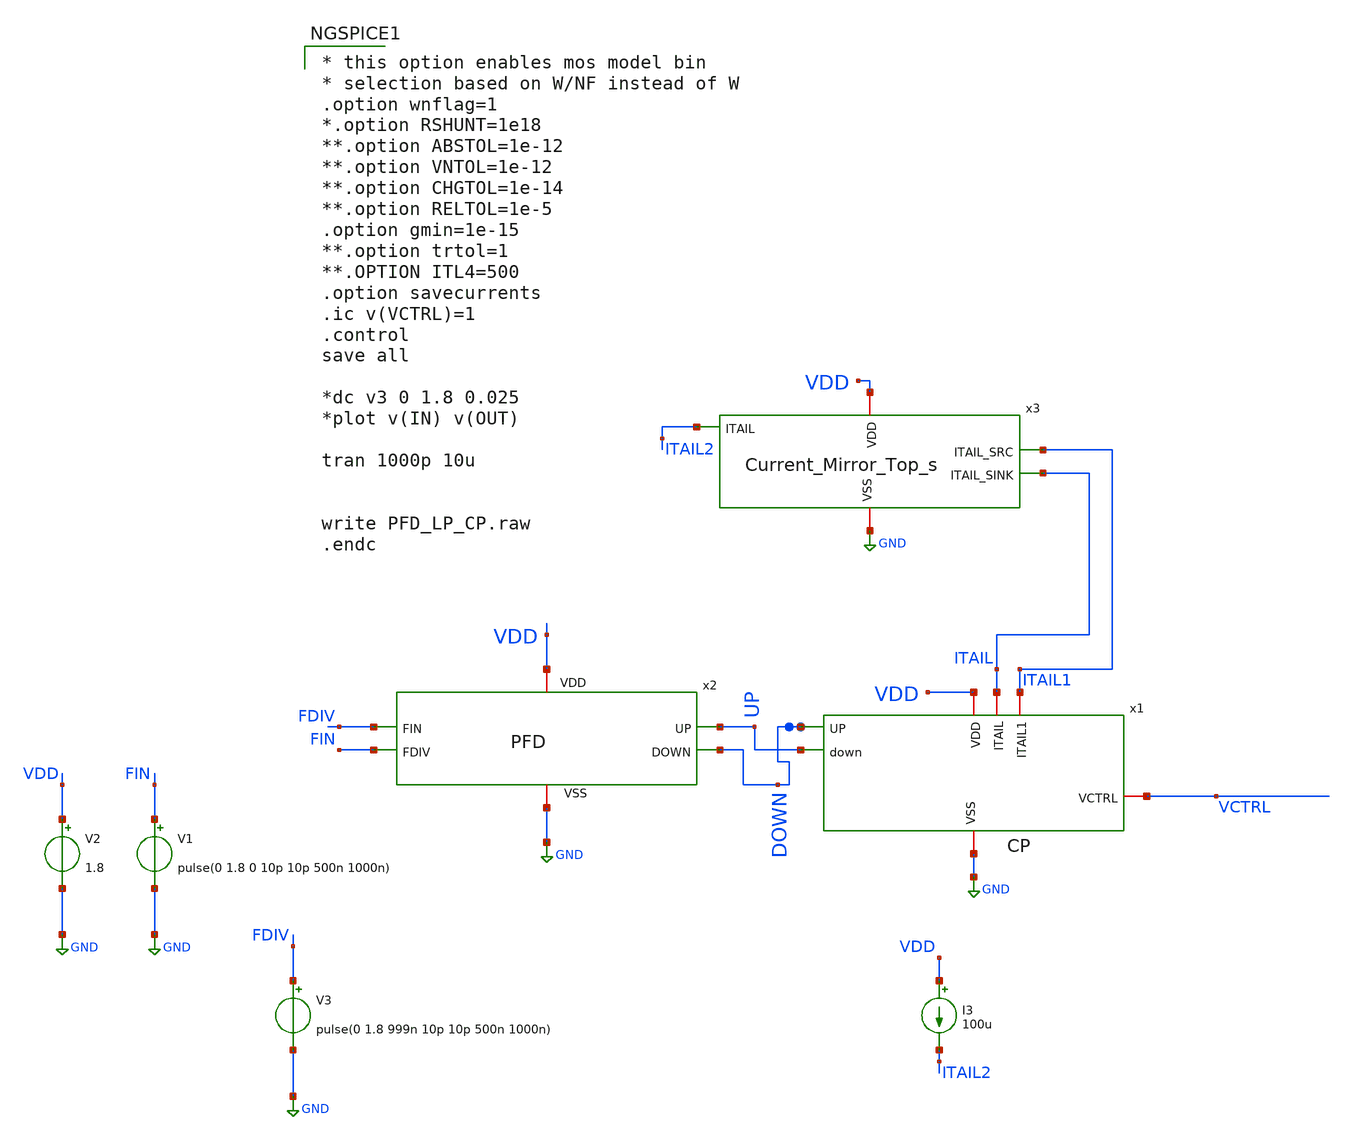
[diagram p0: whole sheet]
** sch_path: Xschem/PLL_TOP/PFD_LP_CP.sch
**.subckt PFD_LP_CP
x1 VDD ITAIL ITAIL1 VCTRL DOWN UP GND CP
V2 VDD GND 1.8
V1 FIN GND pulse(0 1.8 0 10p 10p 500n 1000n)
V3 FDIV GND pulse(0 1.8 999n 10p 10p 500n 1000n)
x2 VDD GND FDIV FIN UP DOWN PFD
x3 VDD ITAIL2 ITAIL1 ITAIL GND Current_Mirror_Top_s
I3 VDD ITAIL2 100u
**** begin user architecture code

** opencircuitdesign pdks install
.lib $::SKYWATER_MODELS/sky130.lib.spice tt



* this option enables mos model bin
* selection based on W/NF instead of W
.option wnflag=1
*.option RSHUNT=1e18
**.option ABSTOL=1e-12
**.option VNTOL=1e-12
**.option CHGTOL=1e-14
**.option RELTOL=1e-5
.option gmin=1e-15
**.option trtol=1
**.OPTION ITL4=500
.option savecurrents
.ic v(VCTRL)=1
.control
save all

*dc v3 0 1.8 0.025
*plot v(IN) v(OUT)

tran 1000p 10u


write PFD_LP_CP.raw
.endc


**** end user architecture code
**.ends

* expanding   symbol:  CP.sym # of pins=7
** sym_path: CP.sym
** sch_path: CP.sch
.subckt CP VDD ITAIL ITAIL1 VCTRL UP down VSS
*.ipin UP
*.ipin down
*.iopin VCTRL
*.iopin VDD
*.iopin VSS
*.iopin ITAIL1
*.iopin ITAIL
XM8 net2 UP VDD VDD sky130_fd_pr__pfet_01v8 L=0.5 W=1 nf=1 ad='int((nf+1)/2) * W/nf * 0.29' as='int((nf+2)/2) * W/nf * 0.29'
+ pd='2*int((nf+1)/2) * (W/nf + 0.29)' ps='2*int((nf+2)/2) * (W/nf + 0.29)' nrd='0.29 / W' nrs='0.29 / W'
+ sa=0 sb=0 sd=0 mult=1 m=1
XM1 net1 net2 VDD VDD sky130_fd_pr__pfet_01v8 L=0.5 W=3 nf=1 ad='int((nf+1)/2) * W/nf * 0.29' as='int((nf+2)/2) * W/nf * 0.29'
+ pd='2*int((nf+1)/2) * (W/nf + 0.29)' ps='2*int((nf+2)/2) * (W/nf + 0.29)' nrd='0.29 / W' nrs='0.29 / W'
+ sa=0 sb=0 sd=0 mult=1 m=1
XM10 net2 UP VSS VSS sky130_fd_pr__nfet_01v8 L=0.5 W=0.5 nf=1 ad='int((nf+1)/2) * W/nf * 0.29' as='int((nf+2)/2) * W/nf * 0.29'
+ pd='2*int((nf+1)/2) * (W/nf + 0.29)' ps='2*int((nf+2)/2) * (W/nf + 0.29)' nrd='0.29 / W' nrs='0.29 / W'
+ sa=0 sb=0 sd=0 mult=1 m=1
XM2 VCTRL ITAIL net1 VDD sky130_fd_pr__pfet_01v8 L=0.5 W=2.5 nf=1 ad='int((nf+1)/2) * W/nf * 0.29' as='int((nf+2)/2) * W/nf * 0.29'
+ pd='2*int((nf+1)/2) * (W/nf + 0.29)' ps='2*int((nf+2)/2) * (W/nf + 0.29)' nrd='0.29 / W' nrs='0.29 / W'
+ sa=0 sb=0 sd=0 mult=1 m=1
XM3 ITAIL ITAIL VDD VDD sky130_fd_pr__pfet_01v8 L=0.5 W=2.5 nf=1 ad='int((nf+1)/2) * W/nf * 0.29' as='int((nf+2)/2) * W/nf * 0.29'
+ pd='2*int((nf+1)/2) * (W/nf + 0.29)' ps='2*int((nf+2)/2) * (W/nf + 0.29)' nrd='0.29 / W' nrs='0.29 / W'
+ sa=0 sb=0 sd=0 mult=1 m=1
XM5 ITAIL1 ITAIL1 VSS VSS sky130_fd_pr__nfet_01v8 L=0.5 W=1.5 nf=1 ad='int((nf+1)/2) * W/nf * 0.29' as='int((nf+2)/2) * W/nf * 0.29'
+ pd='2*int((nf+1)/2) * (W/nf + 0.29)' ps='2*int((nf+2)/2) * (W/nf + 0.29)' nrd='0.29 / W' nrs='0.29 / W'
+ sa=0 sb=0 sd=0 mult=1 m=1
XM6 VCTRL ITAIL1 net3 VSS sky130_fd_pr__nfet_01v8 L=0.5 W=1.5 nf=1 ad='int((nf+1)/2) * W/nf * 0.29' as='int((nf+2)/2) * W/nf * 0.29'
+ pd='2*int((nf+1)/2) * (W/nf + 0.29)' ps='2*int((nf+2)/2) * (W/nf + 0.29)' nrd='0.29 / W' nrs='0.29 / W'
+ sa=0 sb=0 sd=0 mult=1 m=1
XM4 net3 down VSS VSS sky130_fd_pr__nfet_01v8 L=0.5 W=1.5 nf=1 ad='int((nf+1)/2) * W/nf * 0.29' as='int((nf+2)/2) * W/nf * 0.29'
+ pd='2*int((nf+1)/2) * (W/nf + 0.29)' ps='2*int((nf+2)/2) * (W/nf + 0.29)' nrd='0.29 / W' nrs='0.29 / W'
+ sa=0 sb=0 sd=0 mult=1 m=1
.ends


* expanding   symbol:  PFD.sym # of pins=6
** sym_path: xschem/PFD.sym
** sch_path: xschem/PFD.sch
.subckt PFD VDD VSS FDIV FIN UP DOWN
*.ipin FDIV
*.ipin FIN
*.opin UP
*.opin DOWN
*.iopin VSS
*.iopin VDD
XM2 A FIN VDD VDD sky130_fd_pr__pfet_01v8 L=0.15 W=0.6 nf=1 ad='int((nf+1)/2) * W/nf * 0.29' as='int((nf+2)/2) * W/nf * 0.29'
+ pd='2*int((nf+1)/2) * (W/nf + 0.29)' ps='2*int((nf+2)/2) * (W/nf + 0.29)' nrd='0.29 / W' nrs='0.29 / W'
+ sa=0 sb=0 sd=0 mult=1 m=1
XM3 x1 A VDD VDD sky130_fd_pr__pfet_01v8 L=0.15 W=2.4 nf=1 ad='int((nf+1)/2) * W/nf * 0.29' as='int((nf+2)/2) * W/nf * 0.29'
+ pd='2*int((nf+1)/2) * (W/nf + 0.29)' ps='2*int((nf+2)/2) * (W/nf + 0.29)' nrd='0.29 / W' nrs='0.29 / W'
+ sa=0 sb=0 sd=0 mult=1 m=1
XM4 x1 x1 net1 VDD sky130_fd_pr__pfet_01v8 L=0.15 W=0.9 nf=1 ad='int((nf+1)/2) * W/nf * 0.29' as='int((nf+2)/2) * W/nf * 0.29'
+ pd='2*int((nf+1)/2) * (W/nf + 0.29)' ps='2*int((nf+2)/2) * (W/nf + 0.29)' nrd='0.29 / W' nrs='0.29 / W'
+ sa=0 sb=0 sd=0 mult=1 m=1
XM5 net1 x2 VDD VDD sky130_fd_pr__pfet_01v8 L=0.15 W=0.9 nf=1 ad='int((nf+1)/2) * W/nf * 0.29' as='int((nf+2)/2) * W/nf * 0.29'
+ pd='2*int((nf+1)/2) * (W/nf + 0.29)' ps='2*int((nf+2)/2) * (W/nf + 0.29)' nrd='0.29 / W' nrs='0.29 / W'
+ sa=0 sb=0 sd=0 mult=1 m=1
XM6 x3 x1 VDD VDD sky130_fd_pr__pfet_01v8 L=0.3 W=0.9 nf=1 ad='int((nf+1)/2) * W/nf * 0.29' as='int((nf+2)/2) * W/nf * 0.29'
+ pd='2*int((nf+1)/2) * (W/nf + 0.29)' ps='2*int((nf+2)/2) * (W/nf + 0.29)' nrd='0.29 / W' nrs='0.29 / W'
+ sa=0 sb=0 sd=0 mult=1 m=1
XM7 A x1b net2 VSS sky130_fd_pr__nfet_01v8 L=0.3 W=0.6 nf=1 ad='int((nf+1)/2) * W/nf * 0.29' as='int((nf+2)/2) * W/nf * 0.29'
+ pd='2*int((nf+1)/2) * (W/nf + 0.29)' ps='2*int((nf+2)/2) * (W/nf + 0.29)' nrd='0.29 / W' nrs='0.29 / W'
+ sa=0 sb=0 sd=0 mult=1 m=1
XM8 net2 x2b net12 VSS sky130_fd_pr__nfet_01v8 L=0.3 W=0.6 nf=1 ad='int((nf+1)/2) * W/nf * 0.29' as='int((nf+2)/2) * W/nf * 0.29'
+ pd='2*int((nf+1)/2) * (W/nf + 0.29)' ps='2*int((nf+2)/2) * (W/nf + 0.29)' nrd='0.29 / W' nrs='0.29 / W'
+ sa=0 sb=0 sd=0 mult=1 m=1
XM9 x1 FIN net3 VSS sky130_fd_pr__nfet_01v8 L=0.15 W=0.6 nf=1 ad='int((nf+1)/2) * W/nf * 0.29' as='int((nf+2)/2) * W/nf * 0.29'
+ pd='2*int((nf+1)/2) * (W/nf + 0.29)' ps='2*int((nf+2)/2) * (W/nf + 0.29)' nrd='0.29 / W' nrs='0.29 / W'
+ sa=0 sb=0 sd=0 mult=1 m=1
XM10 net3 A VSS VSS sky130_fd_pr__nfet_01v8 L=0.15 W=0.6 nf=1 ad='int((nf+1)/2) * W/nf * 0.29' as='int((nf+2)/2) * W/nf * 0.29'
+ pd='2*int((nf+1)/2) * (W/nf + 0.29)' ps='2*int((nf+2)/2) * (W/nf + 0.29)' nrd='0.29 / W' nrs='0.29 / W'
+ sa=0 sb=0 sd=0 mult=1 m=1
XM11 x3 x1 net4 VSS sky130_fd_pr__nfet_01v8 L=0.15 W=0.6 nf=1 ad='int((nf+1)/2) * W/nf * 0.29' as='int((nf+2)/2) * W/nf * 0.29'
+ pd='2*int((nf+1)/2) * (W/nf + 0.29)' ps='2*int((nf+2)/2) * (W/nf + 0.29)' nrd='0.29 / W' nrs='0.29 / W'
+ sa=0 sb=0 sd=0 mult=1 m=1
XM12 net4 x1 VSS VSS sky130_fd_pr__nfet_01v8 L=0.15 W=0.6 nf=1 ad='int((nf+1)/2) * W/nf * 0.29' as='int((nf+2)/2) * W/nf * 0.29'
+ pd='2*int((nf+1)/2) * (W/nf + 0.29)' ps='2*int((nf+2)/2) * (W/nf + 0.29)' nrd='0.29 / W' nrs='0.29 / W'
+ sa=0 sb=0 sd=0 mult=1 m=1
XM13 x3 x2b VSS VSS sky130_fd_pr__nfet_01v8 L=0.3 W=2.4 nf=1 ad='int((nf+1)/2) * W/nf * 0.29' as='int((nf+2)/2) * W/nf * 0.29'
+ pd='2*int((nf+1)/2) * (W/nf + 0.29)' ps='2*int((nf+2)/2) * (W/nf + 0.29)' nrd='0.29 / W' nrs='0.29 / W'
+ sa=0 sb=0 sd=0 mult=1 m=1
XM15 B FDIV VDD VDD sky130_fd_pr__pfet_01v8 L=0.15 W=0.6 nf=1 ad='int((nf+1)/2) * W/nf * 0.29' as='int((nf+2)/2) * W/nf * 0.29'
+ pd='2*int((nf+1)/2) * (W/nf + 0.29)' ps='2*int((nf+2)/2) * (W/nf + 0.29)' nrd='0.29 / W' nrs='0.29 / W'
+ sa=0 sb=0 sd=0 mult=1 m=1
XM16 x2 B VDD VDD sky130_fd_pr__pfet_01v8 L=0.15 W=2.4 nf=1 ad='int((nf+1)/2) * W/nf * 0.29' as='int((nf+2)/2) * W/nf * 0.29'
+ pd='2*int((nf+1)/2) * (W/nf + 0.29)' ps='2*int((nf+2)/2) * (W/nf + 0.29)' nrd='0.29 / W' nrs='0.29 / W'
+ sa=0 sb=0 sd=0 mult=1 m=1
XM17 x2 x2 net5 VDD sky130_fd_pr__pfet_01v8 L=0.15 W=0.9 nf=1 ad='int((nf+1)/2) * W/nf * 0.29' as='int((nf+2)/2) * W/nf * 0.29'
+ pd='2*int((nf+1)/2) * (W/nf + 0.29)' ps='2*int((nf+2)/2) * (W/nf + 0.29)' nrd='0.29 / W' nrs='0.29 / W'
+ sa=0 sb=0 sd=0 mult=1 m=1
XM18 net5 x1 VDD VDD sky130_fd_pr__pfet_01v8 L=0.15 W=0.9 nf=1 ad='int((nf+1)/2) * W/nf * 0.29' as='int((nf+2)/2) * W/nf * 0.29'
+ pd='2*int((nf+1)/2) * (W/nf + 0.29)' ps='2*int((nf+2)/2) * (W/nf + 0.29)' nrd='0.29 / W' nrs='0.29 / W'
+ sa=0 sb=0 sd=0 mult=1 m=1
XM19 x4 x2 VDD VDD sky130_fd_pr__pfet_01v8 L=0.3 W=0.9 nf=1 ad='int((nf+1)/2) * W/nf * 0.29' as='int((nf+2)/2) * W/nf * 0.29'
+ pd='2*int((nf+1)/2) * (W/nf + 0.29)' ps='2*int((nf+2)/2) * (W/nf + 0.29)' nrd='0.29 / W' nrs='0.29 / W'
+ sa=0 sb=0 sd=0 mult=1 m=1
XM20 B x2b net6 VSS sky130_fd_pr__nfet_01v8 L=0.3 W=0.6 nf=1 ad='int((nf+1)/2) * W/nf * 0.29' as='int((nf+2)/2) * W/nf * 0.29'
+ pd='2*int((nf+1)/2) * (W/nf + 0.29)' ps='2*int((nf+2)/2) * (W/nf + 0.29)' nrd='0.29 / W' nrs='0.29 / W'
+ sa=0 sb=0 sd=0 mult=1 m=1
XM21 net6 x1b net11 VSS sky130_fd_pr__nfet_01v8 L=0.3 W=0.6 nf=1 ad='int((nf+1)/2) * W/nf * 0.29' as='int((nf+2)/2) * W/nf * 0.29'
+ pd='2*int((nf+1)/2) * (W/nf + 0.29)' ps='2*int((nf+2)/2) * (W/nf + 0.29)' nrd='0.29 / W' nrs='0.29 / W'
+ sa=0 sb=0 sd=0 mult=1 m=1
XM22 x2 FDIV net8 VSS sky130_fd_pr__nfet_01v8 L=0.15 W=0.6 nf=1 ad='int((nf+1)/2) * W/nf * 0.29' as='int((nf+2)/2) * W/nf * 0.29'
+ pd='2*int((nf+1)/2) * (W/nf + 0.29)' ps='2*int((nf+2)/2) * (W/nf + 0.29)' nrd='0.29 / W' nrs='0.29 / W'
+ sa=0 sb=0 sd=0 mult=1 m=1
XM23 net8 B VSS VSS sky130_fd_pr__nfet_01v8 L=0.15 W=0.6 nf=1 ad='int((nf+1)/2) * W/nf * 0.29' as='int((nf+2)/2) * W/nf * 0.29'
+ pd='2*int((nf+1)/2) * (W/nf + 0.29)' ps='2*int((nf+2)/2) * (W/nf + 0.29)' nrd='0.29 / W' nrs='0.29 / W'
+ sa=0 sb=0 sd=0 mult=1 m=1
XM24 x4 x2 net7 VSS sky130_fd_pr__nfet_01v8 L=0.15 W=0.6 nf=1 ad='int((nf+1)/2) * W/nf * 0.29' as='int((nf+2)/2) * W/nf * 0.29'
+ pd='2*int((nf+1)/2) * (W/nf + 0.29)' ps='2*int((nf+2)/2) * (W/nf + 0.29)' nrd='0.29 / W' nrs='0.29 / W'
+ sa=0 sb=0 sd=0 mult=1 m=1
XM25 net7 x2 VSS VSS sky130_fd_pr__nfet_01v8 L=0.15 W=0.6 nf=1 ad='int((nf+1)/2) * W/nf * 0.29' as='int((nf+2)/2) * W/nf * 0.29'
+ pd='2*int((nf+1)/2) * (W/nf + 0.29)' ps='2*int((nf+2)/2) * (W/nf + 0.29)' nrd='0.29 / W' nrs='0.29 / W'
+ sa=0 sb=0 sd=0 mult=1 m=1
XM26 x4 x1b VSS VSS sky130_fd_pr__nfet_01v8 L=0.3 W=2.4 nf=1 ad='int((nf+1)/2) * W/nf * 0.29' as='int((nf+2)/2) * W/nf * 0.29'
+ pd='2*int((nf+1)/2) * (W/nf + 0.29)' ps='2*int((nf+2)/2) * (W/nf + 0.29)' nrd='0.29 / W' nrs='0.29 / W'
+ sa=0 sb=0 sd=0 mult=1 m=1
XM1 net11 FDIV VSS VSS sky130_fd_pr__nfet_01v8 L=0.3 W=0.6 nf=1 ad='int((nf+1)/2) * W/nf * 0.29' as='int((nf+2)/2) * W/nf * 0.29'
+ pd='2*int((nf+1)/2) * (W/nf + 0.29)' ps='2*int((nf+2)/2) * (W/nf + 0.29)' nrd='0.29 / W' nrs='0.29 / W'
+ sa=0 sb=0 sd=0 mult=1 m=1
XM14 net12 FIN VSS VSS sky130_fd_pr__nfet_01v8 L=0.3 W=0.6 nf=1 ad='int((nf+1)/2) * W/nf * 0.29' as='int((nf+2)/2) * W/nf * 0.29'
+ pd='2*int((nf+1)/2) * (W/nf + 0.29)' ps='2*int((nf+2)/2) * (W/nf + 0.29)' nrd='0.29 / W' nrs='0.29 / W'
+ sa=0 sb=0 sd=0 mult=1 m=1
x1 VDD VSS x1 x1b PFD_INV
x2 VDD VSS x2 x2b PFD_INV
x3 VDD VSS x3 net10 PFD_INV
x5 VDD VSS x4 net9 PFD_INV
x6 VDD VSS net9 DOWN PFD_INV
x4 VDD VSS net10 UP PFD_INV
.ends


* expanding   symbol:  /home/shahid/Sky130Projects/TOP/Current_Mirror_Top_s.sym # of pins=5
** sym_path: /home/shahid/Sky130Projects/TOP/Current_Mirror_Top_s.sym
** sch_path: /home/shahid/Sky130Projects/TOP/Current_Mirror_Top_s.sch
.subckt Current_Mirror_Top_s VDD ITAIL ITAIL_SRC ITAIL_SINK VSS
*.ipin ITAIL
*.iopin VDD
*.iopin VSS
*.opin ITAIL_SRC
*.opin ITAIL_SINK
XM5 ITAIL_SINK G_sink_up net7 VSS sky130_fd_pr__nfet_01v8 L=0.5 W=5 nf=1 ad='int((nf+1)/2) * W/nf * 0.29'
+ as='int((nf+2)/2) * W/nf * 0.29' pd='2*int((nf+1)/2) * (W/nf + 0.29)' ps='2*int((nf+2)/2) * (W/nf + 0.29)'
+ nrd='0.29 / W' nrs='0.29 / W' sa=0 sb=0 sd=0 mult=1 m=1
XM6 net7 G_sink_dn VSS VSS sky130_fd_pr__nfet_01v8 L=0.5 W=5 nf=1 ad='int((nf+1)/2) * W/nf * 0.29' as='int((nf+2)/2) * W/nf * 0.29'
+ pd='2*int((nf+1)/2) * (W/nf + 0.29)' ps='2*int((nf+2)/2) * (W/nf + 0.29)' nrd='0.29 / W' nrs='0.29 / W'
+ sa=0 sb=0 sd=0 mult=1 m=1
XM11 G_source_dn G_sink_up net6 VSS sky130_fd_pr__nfet_01v8 L=0.5 W=5 nf=1 ad='int((nf+1)/2) * W/nf * 0.29'
+ as='int((nf+2)/2) * W/nf * 0.29' pd='2*int((nf+1)/2) * (W/nf + 0.29)' ps='2*int((nf+2)/2) * (W/nf + 0.29)'
+ nrd='0.29 / W' nrs='0.29 / W' sa=0 sb=0 sd=0 mult=1 m=1
XM12 net6 G_sink_dn VSS VSS sky130_fd_pr__nfet_01v8 L=0.5 W=5 nf=1 ad='int((nf+1)/2) * W/nf * 0.29' as='int((nf+2)/2) * W/nf * 0.29'
+ pd='2*int((nf+1)/2) * (W/nf + 0.29)' ps='2*int((nf+2)/2) * (W/nf + 0.29)' nrd='0.29 / W' nrs='0.29 / W'
+ sa=0 sb=0 sd=0 mult=1 m=1
XM15 G_sink_up G_sink_up G_sink_dn VSS sky130_fd_pr__nfet_01v8 L=0.5 W=5 nf=1 ad='int((nf+1)/2) * W/nf * 0.29'
+ as='int((nf+2)/2) * W/nf * 0.29' pd='2*int((nf+1)/2) * (W/nf + 0.29)' ps='2*int((nf+2)/2) * (W/nf + 0.29)'
+ nrd='0.29 / W' nrs='0.29 / W' sa=0 sb=0 sd=0 mult=1 m=1
XM16 G_sink_dn G_sink_dn VSS VSS sky130_fd_pr__nfet_01v8 L=0.5 W=5 nf=1 ad='int((nf+1)/2) * W/nf * 0.29'
+ as='int((nf+2)/2) * W/nf * 0.29' pd='2*int((nf+1)/2) * (W/nf + 0.29)' ps='2*int((nf+2)/2) * (W/nf + 0.29)'
+ nrd='0.29 / W' nrs='0.29 / W' sa=0 sb=0 sd=0 mult=1 m=1
XM1 net2 ITAIL net1 VSS sky130_fd_pr__nfet_01v8 L=0.5 W=20 nf=1 ad='int((nf+1)/2) * W/nf * 0.29' as='int((nf+2)/2) * W/nf * 0.29'
+ pd='2*int((nf+1)/2) * (W/nf + 0.29)' ps='2*int((nf+2)/2) * (W/nf + 0.29)' nrd='0.29 / W' nrs='0.29 / W'
+ sa=0 sb=0 sd=0 mult=1 m=1
XM2 net1 net5 VSS VSS sky130_fd_pr__nfet_01v8 L=0.5 W=20 nf=1 ad='int((nf+1)/2) * W/nf * 0.29' as='int((nf+2)/2) * W/nf * 0.29'
+ pd='2*int((nf+1)/2) * (W/nf + 0.29)' ps='2*int((nf+2)/2) * (W/nf + 0.29)' nrd='0.29 / W' nrs='0.29 / W'
+ sa=0 sb=0 sd=0 mult=1 m=1
XM3 net5 net5 VSS VSS sky130_fd_pr__nfet_01v8 L=0.5 W=20 nf=1 ad='int((nf+1)/2) * W/nf * 0.29' as='int((nf+2)/2) * W/nf * 0.29'
+ pd='2*int((nf+1)/2) * (W/nf + 0.29)' ps='2*int((nf+2)/2) * (W/nf + 0.29)' nrd='0.29 / W' nrs='0.29 / W'
+ sa=0 sb=0 sd=0 mult=1 m=1
XM4 ITAIL ITAIL net5 VSS sky130_fd_pr__nfet_01v8 L=0.5 W=20 nf=1 ad='int((nf+1)/2) * W/nf * 0.29' as='int((nf+2)/2) * W/nf * 0.29'
+ pd='2*int((nf+1)/2) * (W/nf + 0.29)' ps='2*int((nf+2)/2) * (W/nf + 0.29)' nrd='0.29 / W' nrs='0.29 / W'
+ sa=0 sb=0 sd=0 mult=1 m=1
XM13 ITAIL_SRC G_source_dn net8 VDD sky130_fd_pr__pfet_01v8 L=0.5 W=5 nf=1 ad='int((nf+1)/2) * W/nf * 0.29'
+ as='int((nf+2)/2) * W/nf * 0.29' pd='2*int((nf+1)/2) * (W/nf + 0.29)' ps='2*int((nf+2)/2) * (W/nf + 0.29)'
+ nrd='0.29 / W' nrs='0.29 / W' sa=0 sb=0 sd=0 mult=1 m=1
XM14 net8 G_source_up VDD VDD sky130_fd_pr__pfet_01v8 L=0.5 W=5 nf=1 ad='int((nf+1)/2) * W/nf * 0.29'
+ as='int((nf+2)/2) * W/nf * 0.29' pd='2*int((nf+1)/2) * (W/nf + 0.29)' ps='2*int((nf+2)/2) * (W/nf + 0.29)'
+ nrd='0.29 / W' nrs='0.29 / W' sa=0 sb=0 sd=0 mult=1 m=1
XM17 G_source_up G_source_up VDD VDD sky130_fd_pr__pfet_01v8 L=0.5 W=5 nf=1 ad='int((nf+1)/2) * W/nf * 0.29'
+ as='int((nf+2)/2) * W/nf * 0.29' pd='2*int((nf+1)/2) * (W/nf + 0.29)' ps='2*int((nf+2)/2) * (W/nf + 0.29)'
+ nrd='0.29 / W' nrs='0.29 / W' sa=0 sb=0 sd=0 mult=1 m=1
XM18 G_source_dn G_source_dn G_source_up VDD sky130_fd_pr__pfet_01v8 L=0.5 W=5 nf=1 ad='int((nf+1)/2) * W/nf * 0.29'
+ as='int((nf+2)/2) * W/nf * 0.29' pd='2*int((nf+1)/2) * (W/nf + 0.29)' ps='2*int((nf+2)/2) * (W/nf + 0.29)'
+ nrd='0.29 / W' nrs='0.29 / W' sa=0 sb=0 sd=0 mult=1 m=1
XM9 G_sink_up net2 net4 VDD sky130_fd_pr__pfet_01v8 L=0.5 W=4 nf=1 ad='int((nf+1)/2) * W/nf * 0.29' as='int((nf+2)/2) * W/nf * 0.29'
+ pd='2*int((nf+1)/2) * (W/nf + 0.29)' ps='2*int((nf+2)/2) * (W/nf + 0.29)' nrd='0.29 / W' nrs='0.29 / W'
+ sa=0 sb=0 sd=0 mult=1 m=1
XM10 net4 net3 VDD VDD sky130_fd_pr__pfet_01v8 L=0.5 W=4 nf=1 ad='int((nf+1)/2) * W/nf * 0.29' as='int((nf+2)/2) * W/nf * 0.29'
+ pd='2*int((nf+1)/2) * (W/nf + 0.29)' ps='2*int((nf+2)/2) * (W/nf + 0.29)' nrd='0.29 / W' nrs='0.29 / W'
+ sa=0 sb=0 sd=0 mult=1 m=1
XM7 net2 net2 net3 VDD sky130_fd_pr__pfet_01v8 L=0.5 W=20 nf=1 ad='int((nf+1)/2) * W/nf * 0.29' as='int((nf+2)/2) * W/nf * 0.29'
+ pd='2*int((nf+1)/2) * (W/nf + 0.29)' ps='2*int((nf+2)/2) * (W/nf + 0.29)' nrd='0.29 / W' nrs='0.29 / W'
+ sa=0 sb=0 sd=0 mult=1 m=1
XM8 net3 net3 VDD VDD sky130_fd_pr__pfet_01v8 L=0.5 W=20 nf=1 ad='int((nf+1)/2) * W/nf * 0.29' as='int((nf+2)/2) * W/nf * 0.29'
+ pd='2*int((nf+1)/2) * (W/nf + 0.29)' ps='2*int((nf+2)/2) * (W/nf + 0.29)' nrd='0.29 / W' nrs='0.29 / W'
+ sa=0 sb=0 sd=0 mult=1 m=1
.ends


* expanding   symbol:  PFD_INV.sym # of pins=4
** sym_path: PFD_INV.sym
** sch_path: PFD_INV.sch
.subckt PFD_INV VDD VSS IN OUT
*.iopin VDD
*.iopin VSS
*.ipin IN
*.opin OUT
XM1 OUT IN VDD VDD sky130_fd_pr__pfet_01v8 L=0.15 W=0.8 nf=1 ad='int((nf+1)/2) * W/nf * 0.29' as='int((nf+2)/2) * W/nf * 0.29'
+ pd='2*int((nf+1)/2) * (W/nf + 0.29)' ps='2*int((nf+2)/2) * (W/nf + 0.29)' nrd='0.29 / W' nrs='0.29 / W'
+ sa=0 sb=0 sd=0 mult=1 m=1
XM3 OUT IN VSS VSS sky130_fd_pr__nfet_01v8 L=0.15 W=0.4 nf=1 ad='int((nf+1)/2) * W/nf * 0.29' as='int((nf+2)/2) * W/nf * 0.29'
+ pd='2*int((nf+1)/2) * (W/nf + 0.29)' ps='2*int((nf+2)/2) * (W/nf + 0.29)' nrd='0.29 / W' nrs='0.29 / W'
+ sa=0 sb=0 sd=0 mult=1 m=1
.ends

.GLOBAL GND
.end
